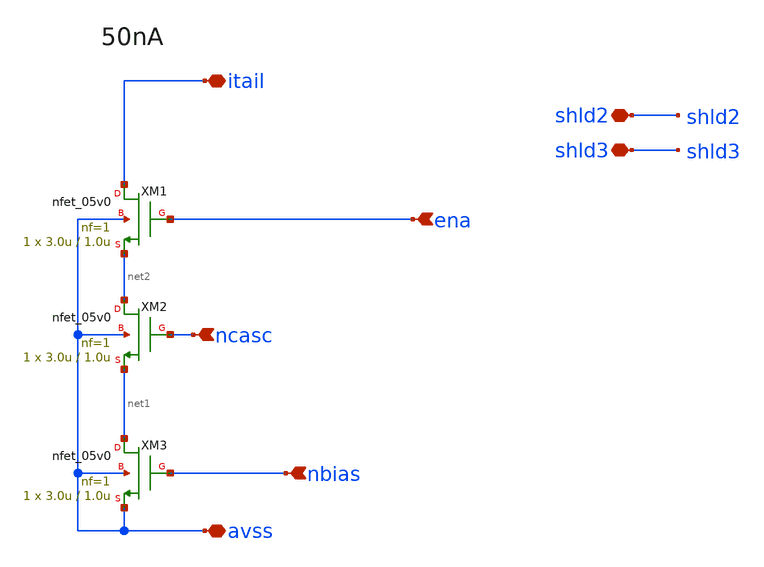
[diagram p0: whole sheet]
** sch_path: projects/programmable_transceiver_platform/analog/core_support/biasgen/xschem/bias_nstack.sch
**.subckt bias_nstack avss ena nbias itail ncasc shld2 shld3
*.iopin avss
*.ipin ena
*.ipin nbias
*.iopin itail
*.ipin ncasc
*.iopin shld2
*.iopin shld3
XM1 itail ena net2 avss nfet_05v0 L=1.0u W=3.0u nf=1 ad='int((nf+1)/2) * W/nf * 0.18u' as='int((nf+2)/2) * W/nf * 0.18u'
+ pd='2*int((nf+1)/2) * (W/nf + 0.18u)' ps='2*int((nf+2)/2) * (W/nf + 0.18u)' nrd='0.18u / W' nrs='0.18u / W'
+ sa=0 sb=0 sd=0 m=1
XM2 net2 ncasc net1 avss nfet_05v0 L=1.0u W=3.0u nf=1 ad='int((nf+1)/2) * W/nf * 0.18u' as='int((nf+2)/2) * W/nf * 0.18u'
+ pd='2*int((nf+1)/2) * (W/nf + 0.18u)' ps='2*int((nf+2)/2) * (W/nf + 0.18u)' nrd='0.18u / W' nrs='0.18u / W'
+ sa=0 sb=0 sd=0 m=1
XM3 net1 nbias avss avss nfet_05v0 L=1.0u W=3.0u nf=1 ad='int((nf+1)/2) * W/nf * 0.18u' as='int((nf+2)/2) * W/nf * 0.18u'
+ pd='2*int((nf+1)/2) * (W/nf + 0.18u)' ps='2*int((nf+2)/2) * (W/nf + 0.18u)' nrd='0.18u / W' nrs='0.18u / W'
+ sa=0 sb=0 sd=0 m=1
**.ends
.end
